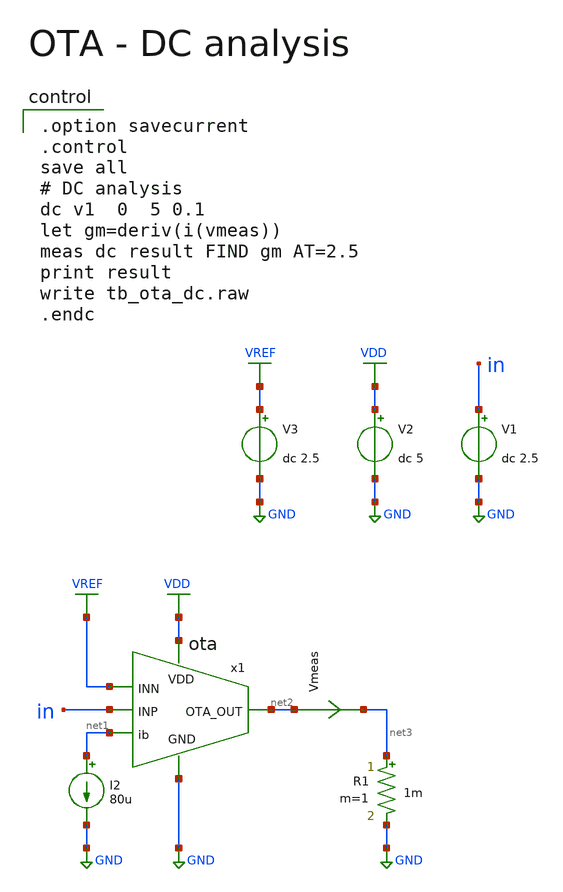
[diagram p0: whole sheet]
** sch_path: member_project/AM_Radio/Yamada3/xschem/tb_ota_dc.sch
**.subckt tb_ota_dc
V2 VDD GND dc 5
V1 in GND dc 2.5
x1 VDD net1 VREF in net2 GND ota
I2 net1 GND 80u
Vmeas net2 net3 0
.save i(vmeas)
R1 net3 GND 1m m=1
V3 VREF GND dc 2.5
**** begin user architecture code

.option savecurrent
.control
save all
# DC analysis
dc v1  0  5 0.1
let gm=deriv(i(vmeas))
meas dc result FIND gm AT=2.5
print result
write tb_ota_dc.raw
.endc

 .include $::LIB/ip62_models
**** end user architecture code
**.ends
.GLOBAL GND
.GLOBAL VDD
.GLOBAL VREF
.end
